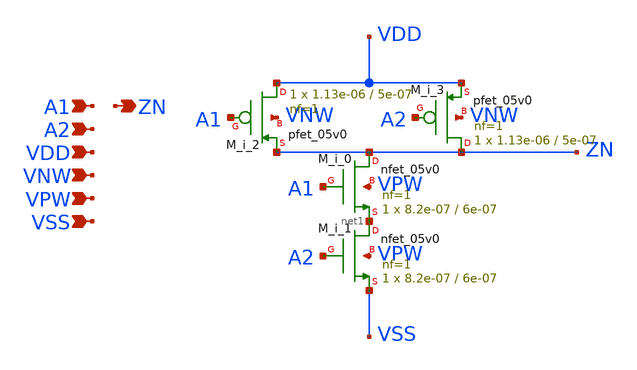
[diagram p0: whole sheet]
** sch_path: schematics/nand2/gf180mcu_fd_sc_mcu7t5v0__nand2_1.sch
**.subckt gf180mcu_fd_sc_mcu7t5v0__nand2_1 A1 A2 ZN VDD VNW VPW VSS
*.ipin A1
*.ipin A2
*.opin ZN
*.ipin VDD
*.ipin VNW
*.ipin VPW
*.ipin VSS
M_i_1 net1 A2 VSS VPW nfet_05v0 L=6e-07 W=8.2e-07 nf=1 ad='int((nf+1)/2) * W/nf * 0.18u' as='int((nf+2)/2) * W/nf * 0.18u'
+ pd='2*int((nf+1)/2) * (W/nf + 0.18u)' ps='2*int((nf+2)/2) * (W/nf + 0.18u)' nrd='0.18u / W' nrs='0.18u / W'
+ sa=0 sb=0 sd=0 m=1
M_i_0 ZN A1 net1 VPW nfet_05v0 L=6e-07 W=8.2e-07 nf=1 ad='int((nf+1)/2) * W/nf * 0.18u' as='int((nf+2)/2) * W/nf * 0.18u'
+ pd='2*int((nf+1)/2) * (W/nf + 0.18u)' ps='2*int((nf+2)/2) * (W/nf + 0.18u)' nrd='0.18u / W' nrs='0.18u / W'
+ sa=0 sb=0 sd=0 m=1
M_i_3 ZN A2 VDD VNW pfet_05v0 L=5e-07 W=1.13e-06 nf=1 ad='int((nf+1)/2) * W/nf * 0.18u' as='int((nf+2)/2) * W/nf * 0.18u'
+ pd='2*int((nf+1)/2) * (W/nf + 0.18u)' ps='2*int((nf+2)/2) * (W/nf + 0.18u)' nrd='0.18u / W' nrs='0.18u / W'
+ sa=0 sb=0 sd=0 m=1
M_i_2 VDD A1 ZN VNW pfet_05v0 L=5e-07 W=1.13e-06 nf=1 ad='int((nf+1)/2) * W/nf * 0.18u' as='int((nf+2)/2) * W/nf * 0.18u'
+ pd='2*int((nf+1)/2) * (W/nf + 0.18u)' ps='2*int((nf+2)/2) * (W/nf + 0.18u)' nrd='0.18u / W' nrs='0.18u / W'
+ sa=0 sb=0 sd=0 m=1
**.ends
.end
